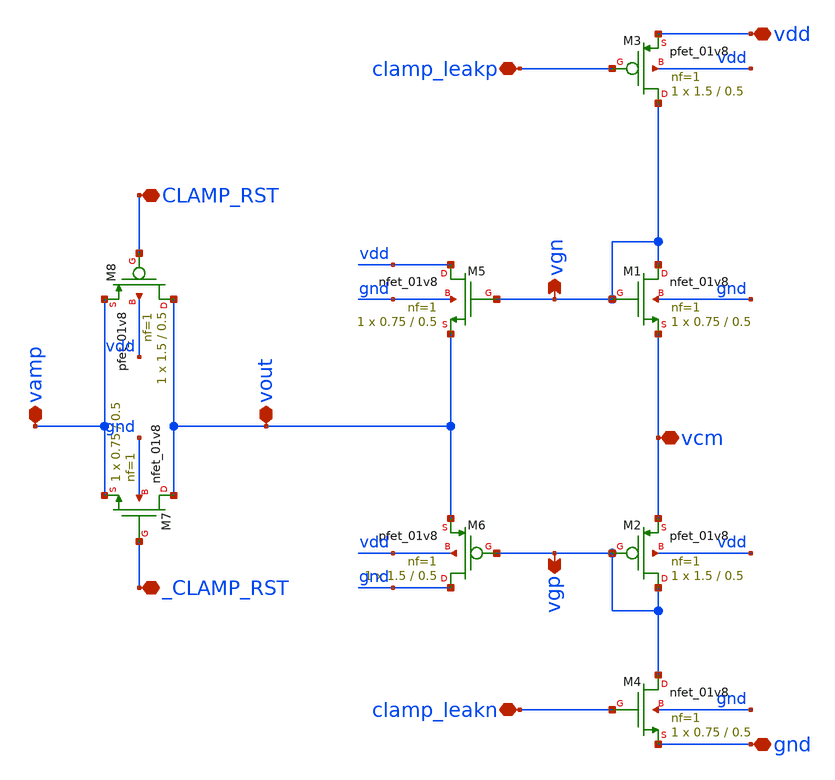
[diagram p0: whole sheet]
** sch_path: analog/xschem/final/col_amp_n_clamp_v1/clamp_qdvs_v2.sch
**.subckt clamp_qdvs_v2 vdd gnd vcm _CLAMP_RST CLAMP_RST clamp_leakp clamp_leakn vout vamp vgn vgp
*.iopin vdd
*.iopin gnd
*.iopin vcm
*.iopin _CLAMP_RST
*.iopin CLAMP_RST
*.iopin clamp_leakp
*.iopin clamp_leakn
*.iopin vout
*.iopin vamp
*.opin vgn
*.opin vgp
XM1 vgn vgn vcm gnd sky130_fd_pr__nfet_01v8 L=0.5 W=0.75 nf=1 ad='int((1 + 1)/2) * 0.75 / 1 * 0.29' as='int((1 + 2)/2) * 0.75 / 1 * 0.29'
+ pd='2*int((1 + 1)/2) * (0.75 / 1 + 0.29)' ps='2*int((1 + 2)/2) * (0.75 / 1 + 0.29)' nrd='0.29 / 0.75 '
+ nrs='0.29 / 0.75 ' sa=0 sb=0 sd=0 mult=1 m=1
XM2 vgp vgp vcm vdd sky130_fd_pr__pfet_01v8 L=0.5 W=1.5 nf=1 ad='int((1 + 1)/2) * 1.5 / 1 * 0.29' as='int((1 + 2)/2) * 1.5 / 1 * 0.29'
+ pd='2*int((1 + 1)/2) * (1.5 / 1 + 0.29)' ps='2*int((1 + 2)/2) * (1.5 / 1 + 0.29)' nrd='0.29 / 1.5 ' nrs='0.29 / 1.5 '
+ sa=0 sb=0 sd=0 mult=1 m=1
XM3 vgn clamp_leakp vdd vdd sky130_fd_pr__pfet_01v8 L=0.5 W=1.5 nf=1 ad='int((1 + 1)/2) * 1.5 / 1 * 0.29'
+ as='int((1 + 2)/2) * 1.5 / 1 * 0.29' pd='2*int((1 + 1)/2) * (1.5 / 1 + 0.29)' ps='2*int((1 + 2)/2) * (1.5 / 1 + 0.29)'
+ nrd='0.29 / 1.5 ' nrs='0.29 / 1.5 ' sa=0 sb=0 sd=0 mult=1 m=1
XM4 vgp clamp_leakn gnd gnd sky130_fd_pr__nfet_01v8 L=0.5 W=0.75 nf=1 ad='int((1 + 1)/2) * 0.75 / 1 * 0.29'
+ as='int((1 + 2)/2) * 0.75 / 1 * 0.29' pd='2*int((1 + 1)/2) * (0.75 / 1 + 0.29)' ps='2*int((1 + 2)/2) * (0.75 / 1 + 0.29)'
+ nrd='0.29 / 0.75 ' nrs='0.29 / 0.75 ' sa=0 sb=0 sd=0 mult=1 m=1
XM5 vdd vgn vout gnd sky130_fd_pr__nfet_01v8 L=0.5 W=0.75 nf=1 ad='int((1 + 1)/2) * 0.75 / 1 * 0.29'
+ as='int((1 + 2)/2) * 0.75 / 1 * 0.29' pd='2*int((1 + 1)/2) * (0.75 / 1 + 0.29)' ps='2*int((1 + 2)/2) * (0.75 / 1 + 0.29)'
+ nrd='0.29 / 0.75 ' nrs='0.29 / 0.75 ' sa=0 sb=0 sd=0 mult=1 m=1
XM6 gnd vgp vout vdd sky130_fd_pr__pfet_01v8 L=0.5 W=1.5 nf=1 ad='int((1 + 1)/2) * 1.5 / 1 * 0.29' as='int((1 + 2)/2) * 1.5 / 1 * 0.29'
+ pd='2*int((1 + 1)/2) * (1.5 / 1 + 0.29)' ps='2*int((1 + 2)/2) * (1.5 / 1 + 0.29)' nrd='0.29 / 1.5 ' nrs='0.29 / 1.5 '
+ sa=0 sb=0 sd=0 mult=1 m=1
XM7 vout _CLAMP_RST vamp gnd sky130_fd_pr__nfet_01v8 L=0.5 W=0.75 nf=1 ad='int((1 + 1)/2) * 0.75 / 1 * 0.29'
+ as='int((1 + 2)/2) * 0.75 / 1 * 0.29' pd='2*int((1 + 1)/2) * (0.75 / 1 + 0.29)' ps='2*int((1 + 2)/2) * (0.75 / 1 + 0.29)'
+ nrd='0.29 / 0.75 ' nrs='0.29 / 0.75 ' sa=0 sb=0 sd=0 mult=1 m=1
XM8 vout CLAMP_RST vamp vdd sky130_fd_pr__pfet_01v8 L=0.5 W=1.5 nf=1 ad='int((1 + 1)/2) * 1.5 / 1 * 0.29'
+ as='int((1 + 2)/2) * 1.5 / 1 * 0.29' pd='2*int((1 + 1)/2) * (1.5 / 1 + 0.29)' ps='2*int((1 + 2)/2) * (1.5 / 1 + 0.29)'
+ nrd='0.29 / 1.5 ' nrs='0.29 / 1.5 ' sa=0 sb=0 sd=0 mult=1 m=1
**.ends
.end
